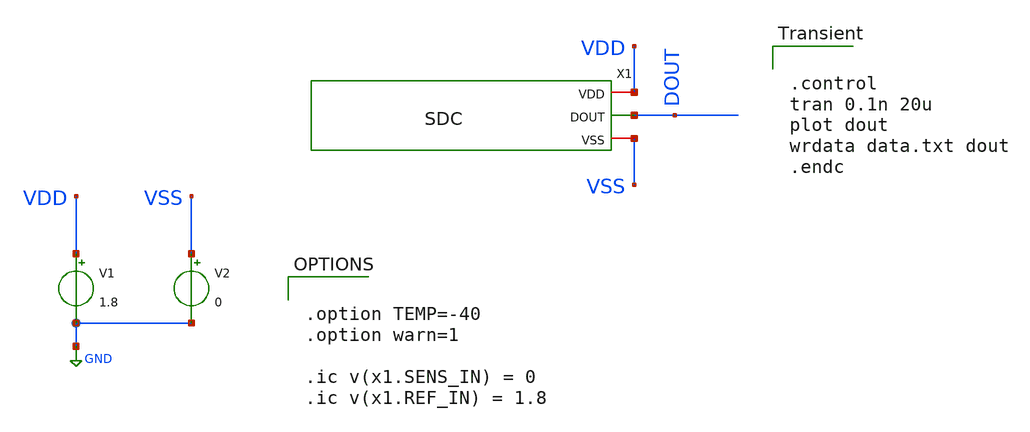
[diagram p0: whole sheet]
** sch_path: modules/SDC/test/transient.sch
**.subckt transient
V1 VDD GND 1.8
V2 VSS GND 0
X1 VDD DOUT VSS SDC
**** begin user architecture code


.control
tran 0.1n 20u
plot dout
wrdata data.txt dout
.endc



.option TEMP=-40
.option warn=1

.ic v(x1.SENS_IN) = 0
.ic v(x1.REF_IN) = 1.8



*.lib $env(PDK_ROOT)/$env(PDK)/libs.tech/combined/sky130.lib.spice tt
.lib $env(PDK_ROOT)/$env(PDK)/libs.tech/ngspice/sky130.lib.spice.tt.red tt

.include $env(PDK_ROOT)/$env(PDK)/libs.ref/sky130_fd_sc_hd/spice/sky130_fd_sc_hd.spice

**** end user architecture code
**.ends
.GLOBAL GND
.end
